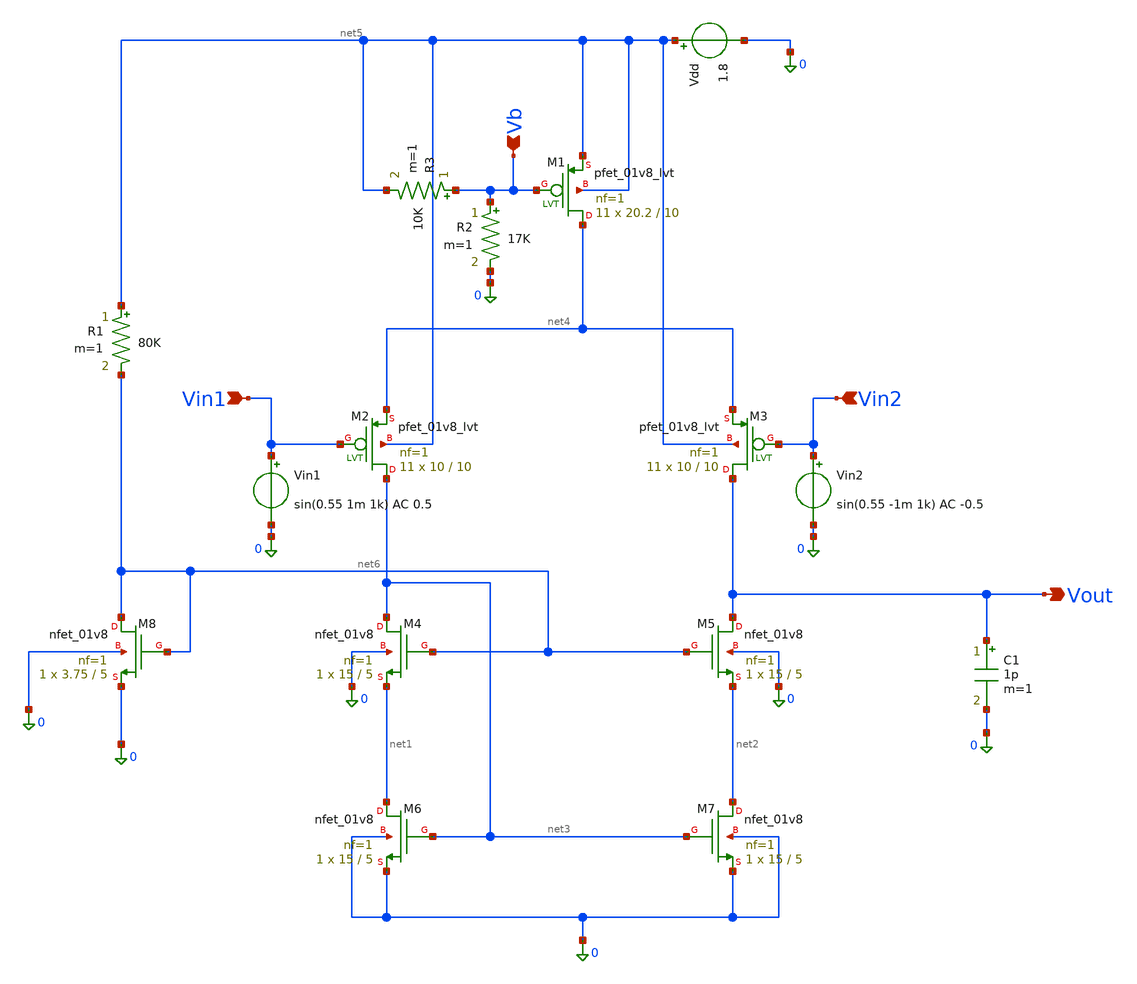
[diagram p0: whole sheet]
** sch_path: Mini_project.sch
**.subckt Mini_project Vin1 Vin2 Vout Vb
*.ipin Vin1
*.ipin Vin2
*.opin Vout
*.ipin Vb
XM2 net3 Vin1 net4 net5 sky130_fd_pr__pfet_01v8_lvt L=10 W=10 nf=1 ad='int((1 + 1)/2) * 10 / 1 * 0.29'
+ as='int((1 + 2)/2) * 10 / 1 * 0.29' pd='2*int((1 + 1)/2) * (10 / 1 + 0.29)' ps='2*int((1 + 2)/2) * (10 / 1 + 0.29)'
+ nrd='0.29 / 10 ' nrs='0.29 / 10 ' sa=0 sb=0 sd=0 mult=11 m=11
XM3 Vout Vin2 net4 net5 sky130_fd_pr__pfet_01v8_lvt L=10 W=10 nf=1 ad='int((1 + 1)/2) * 10 / 1 * 0.29'
+ as='int((1 + 2)/2) * 10 / 1 * 0.29' pd='2*int((1 + 1)/2) * (10 / 1 + 0.29)' ps='2*int((1 + 2)/2) * (10 / 1 + 0.29)'
+ nrd='0.29 / 10 ' nrs='0.29 / 10 ' sa=0 sb=0 sd=0 mult=11 m=11
XM4 net3 net6 net1 0 sky130_fd_pr__nfet_01v8 L=5 W=15 nf=1 ad='int((1 + 1)/2) * 15 / 1 * 0.29' as='int((1 + 2)/2) * 15 / 1 * 0.29'
+ pd='2*int((1 + 1)/2) * (15 / 1 + 0.29)' ps='2*int((1 + 2)/2) * (15 / 1 + 0.29)' nrd='0.29 / 15 ' nrs='0.29 / 15 '
+ sa=0 sb=0 sd=0 mult=1 m=1
XM5 Vout net6 net2 0 sky130_fd_pr__nfet_01v8 L=5 W=15 nf=1 ad='int((1 + 1)/2) * 15 / 1 * 0.29' as='int((1 + 2)/2) * 15 / 1 * 0.29'
+ pd='2*int((1 + 1)/2) * (15 / 1 + 0.29)' ps='2*int((1 + 2)/2) * (15 / 1 + 0.29)' nrd='0.29 / 15 ' nrs='0.29 / 15 '
+ sa=0 sb=0 sd=0 mult=1 m=1
XM6 net1 net3 0 0 sky130_fd_pr__nfet_01v8 L=5 W=15 nf=1 ad='int((1 + 1)/2) * 15 / 1 * 0.29' as='int((1 + 2)/2) * 15 / 1 * 0.29'
+ pd='2*int((1 + 1)/2) * (15 / 1 + 0.29)' ps='2*int((1 + 2)/2) * (15 / 1 + 0.29)' nrd='0.29 / 15 ' nrs='0.29 / 15 '
+ sa=0 sb=0 sd=0 mult=1 m=1
XM7 net2 net3 0 0 sky130_fd_pr__nfet_01v8 L=5 W=15 nf=1 ad='int((1 + 1)/2) * 15 / 1 * 0.29' as='int((1 + 2)/2) * 15 / 1 * 0.29'
+ pd='2*int((1 + 1)/2) * (15 / 1 + 0.29)' ps='2*int((1 + 2)/2) * (15 / 1 + 0.29)' nrd='0.29 / 15 ' nrs='0.29 / 15 '
+ sa=0 sb=0 sd=0 mult=1 m=1
XM8 net6 net6 0 0 sky130_fd_pr__nfet_01v8 L=5 W=3.75 nf=1 ad='int((1 + 1)/2) * 3.75 / 1 * 0.29' as='int((1 + 2)/2) * 3.75 / 1 * 0.29'
+ pd='2*int((1 + 1)/2) * (3.75 / 1 + 0.29)' ps='2*int((1 + 2)/2) * (3.75 / 1 + 0.29)' nrd='0.29 / 3.75 '
+ nrs='0.29 / 3.75 ' sa=0 sb=0 sd=0 mult=1 m=1
Vdd net5 0 1.8
Vin1 Vin1 0 sin(0.55 1m 1k) AC 0.5
Vin2 Vin2 0 sin(0.55 -1m 1k) AC -0.5
R1 net5 net6 80K m=1
C1 Vout 0 1p m=1
XM1 net4 Vb net5 net5 sky130_fd_pr__pfet_01v8_lvt L=10 W=20.2 nf=1 ad='int((1 + 1)/2) * 20.2 / 1 * 0.29'
+ as='int((1 + 2)/2) * 20.2 / 1 * 0.29' pd='2*int((1 + 1)/2) * (20.2 / 1 + 0.29)' ps='2*int((1 + 2)/2) * (20.2 / 1 + 0.29)'
+ nrd='0.29 / 20.2 ' nrs='0.29 / 20.2 ' sa=0 sb=0 sd=0 mult=11 m=11
R2 Vb 0 17K m=1
R3 Vb net5 10K m=1
**** begin user architecture code


.lib /foss/pdks/ciel/sky130/versions/b344c97eacc2aaf8e14ae7e43e2e9dc0871de2c0/sky130A/libs.tech/ngspice/sky130.lib.spice tt

Vtest vt_node 0 dc 0
S1 Vout vt_node ctrl 0 SW1
Vsw ctrl 0 dc 0
.model SW1 SW(Vt=0.5 Vh=0.1 Ron=1m Roff=1e15)

.control
  option temp = 27
  alter vdd dc = 1.8
  set color0=white
  set color1=black
  set color2=red
  set color3=blue

  op
  echo --- Tail Transistor M1 ---
  print @m.xm1.msky130_fd_pr__pfet_01v8_lvt[id]
  print @m.xm1.msky130_fd_pr__pfet_01v8_lvt[vds]
  print @m.xm1.msky130_fd_pr__pfet_01v8_lvt[vdsat]
  print @m.xm1.msky130_fd_pr__pfet_01v8_lvt[vgs]
  print @m.xm1.msky130_fd_pr__pfet_01v8_lvt[vth]
  print @m.xm1.msky130_fd_pr__pfet_01v8_lvt[gm]
  print @m.xm1.msky130_fd_pr__pfet_01v8_lvt[gds]

  echo --- Differential Pair M2 ---
  print @m.xm2.msky130_fd_pr__pfet_01v8_lvt[id]
  print @m.xm2.msky130_fd_pr__pfet_01v8_lvt[vds]
  print @m.xm2.msky130_fd_pr__pfet_01v8_lvt[vdsat]
  print @m.xm2.msky130_fd_pr__pfet_01v8_lvt[vgs]
  print @m.xm2.msky130_fd_pr__pfet_01v8_lvt[vth]
  print @m.xm2.msky130_fd_pr__pfet_01v8_lvt[gm]
  print @m.xm2.msky130_fd_pr__pfet_01v8_lvt[gds]

  echo --- Differential Pair M3 ---
  print @m.xm3.msky130_fd_pr__pfet_01v8_lvt[id]
  print @m.xm3.msky130_fd_pr__pfet_01v8_lvt[vds]
  print @m.xm3.msky130_fd_pr__pfet_01v8_lvt[vdsat]
  print @m.xm3.msky130_fd_pr__pfet_01v8_lvt[vgs]
  print @m.xm3.msky130_fd_pr__pfet_01v8_lvt[vth]
  print @m.xm3.msky130_fd_pr__pfet_01v8_lvt[gm]
  print @m.xm3.msky130_fd_pr__pfet_01v8_lvt[gds]

  echo --- Current Mirror M4 ---
  print @m.xm4.msky130_fd_pr__nfet_01v8[id]
  print @m.xm4.msky130_fd_pr__nfet_01v8[vds]
  print @m.xm4.msky130_fd_pr__nfet_01v8[vdsat]
  print @m.xm4.msky130_fd_pr__nfet_01v8[vgs]
  print @m.xm4.msky130_fd_pr__nfet_01v8[vth]
  print @m.xm4.msky130_fd_pr__nfet_01v8[gm]
  print @m.xm4.msky130_fd_pr__nfet_01v8[gds]

  echo --- Current Mirror M5 ---
  print @m.xm5.msky130_fd_pr__nfet_01v8[id]
  print @m.xm5.msky130_fd_pr__nfet_01v8[vds]
  print @m.xm5.msky130_fd_pr__nfet_01v8[vdsat]
  print @m.xm5.msky130_fd_pr__nfet_01v8[vgs]
  print @m.xm5.msky130_fd_pr__nfet_01v8[vth]
  print @m.xm5.msky130_fd_pr__nfet_01v8[gm]
  print @m.xm5.msky130_fd_pr__nfet_01v8[gds]

  echo --- Cascode Current Mirror M6 ---
  print @m.xm6.msky130_fd_pr__nfet_01v8[id]
  print @m.xm6.msky130_fd_pr__nfet_01v8[vds]
  print @m.xm6.msky130_fd_pr__nfet_01v8[vdsat]
  print @m.xm6.msky130_fd_pr__nfet_01v8[vgs]
  print @m.xm6.msky130_fd_pr__nfet_01v8[vth]
  print @m.xm6.msky130_fd_pr__nfet_01v8[gm]
  print @m.xm6.msky130_fd_pr__nfet_01v8[gds]

  echo --- Cascode Current Mirror M7 ---
  print @m.xm7.msky130_fd_pr__nfet_01v8[id]
  print @m.xm7.msky130_fd_pr__nfet_01v8[vds]
  print @m.xm7.msky130_fd_pr__nfet_01v8[vdsat]
  print @m.xm7.msky130_fd_pr__nfet_01v8[vgs]
  print @m.xm7.msky130_fd_pr__nfet_01v8[vth]
  print @m.xm7.msky130_fd_pr__nfet_01v8[gm]
  print @m.xm7.msky130_fd_pr__nfet_01v8[gds]

  echo --- Bias Transistor M8 ---
  print @m.xm8.msky130_fd_pr__nfet_01v8[id]
  print @m.xm8.msky130_fd_pr__nfet_01v8[vds]
  print @m.xm8.msky130_fd_pr__nfet_01v8[vdsat]
  print @m.xm8.msky130_fd_pr__nfet_01v8[vgs]
  print @m.xm8.msky130_fd_pr__nfet_01v8[vth]
  print @m.xm8.msky130_fd_pr__nfet_01v8[gm]
  print @m.xm8.msky130_fd_pr__nfet_01v8[gds]


* ---------- Power dissipation (DC operating point) ----------

  let i_vdd = -i(vdd)
  let p_diss = 1.8 * i_vdd

  echo --- * Supply current and Power dissipation * ---

  print i_vdd p_diss


* ---------- Transient ----------

  tran 1u 5m

 plot v(vin1) v(vin2) title 'Input: differential sine (1 kHz)'
 plot v(vout) title 'Output: 1 kHz response'



* ---------- Differential : gain, bandwidth, phase margin ----------

  alter Vin1 ac = 0.5
  alter Vin2 ac = -0.5
  ac dec 50 1 10g
  let ad_db = db(v(vout))
  let ad_ph = ph(v(vout)) * 180 / pi
  let ad_ph_rel = ad_ph - ad_ph[0]
  let dist3 = ad_db - (ad_db[0] - 3)
  meas ac f_3dB WHEN dist3=0 CROSS=1
  meas ac f_ugf WHEN ad_db=0 CROSS=1
  meas ac phase_at_ugf FIND ad_ph_rel WHEN ad_db=0 CROSS=1
  let pm_deg = 180 + phase_at_ugf

  echo --- * Differential Gain, Bandwidth, Phase margin * ---
  print ad_db[0] f_3dB f_ugf pm_deg
  plot ad_db title 'Differential Gain Ad (dB)'
  plot ad_ph title 'Differential Phase (deg)'


* ---------- CMRR ----------

  alter Vin1 ac = 1
  alter Vin2 ac = 0
  ac dec 50 1 10g

  alter Vin1 ac = 0
  alter Vin2 ac = 1
  ac dec 50 1 10g


  let Ad_c   = (ac2.v(vout) - ac3.v(vout)) / 2
  let Acm_c  = ac2.v(vout) + ac3.v(vout)
  let cmrr_c = db(Ad_c / Acm_c)

  echo --- * Differential Gain Ad(dB), Common-mode Gain Acm(dB), CMRR(dB) * ---

  print db(Ad_c)[0] db(Acm_c)[0] cmrr_c[0]
  plot db(Ad_c) db(Acm_c) title 'Ad and Acm (dB)'
  plot cmrr_c title 'CMRR (dB)'


  alter Vin1 ac = 0.5
  alter Vin2 ac = -0.5

* ---------- DC transfer ----------
  dc Vin2 0 1.8 0.01
  plot Vout title 'DC transfer Characteristic'

  write miniproject.raw

* ---------- Io vs Vo sweep (M5/M7 cascode mirror output current) ----------
  alter Vsw dc = 1
  save all @m.xm5.msky130_fd_pr__nfet_01v8[id] @m.xm3.msky130_fd_pr__pfet_01v8_lvt[id]
  dc Vtest 0 1.8 0.005

  let Iout = @m.xm5.msky130_fd_pr__nfet_01v8[id]
  let Im3  = -@m.xm3.msky130_fd_pr__pfet_01v8_lvt[id]
  let Vo   = v(vout)

  plot Iout vs Vo title 'Io vs Vo (M5/M7 cascode mirror)' xlabel 'Vout (V)' ylabel 'Iout (A)'
  plot Iout Im3 vs Vo title 'M5 sink vs M3 source' xlabel 'Vout (V)' ylabel 'Current (A)'

  let p_v = -1.8 * i(vdd) * 1e6
  plot p_v vs Vo title 'Power vs output voltage (uW)' xlabel 'Vout (V)' ylabel 'Power (uW)'

  alter Vsw dc = 0
.endc


**** end user architecture code
**.ends
.end
